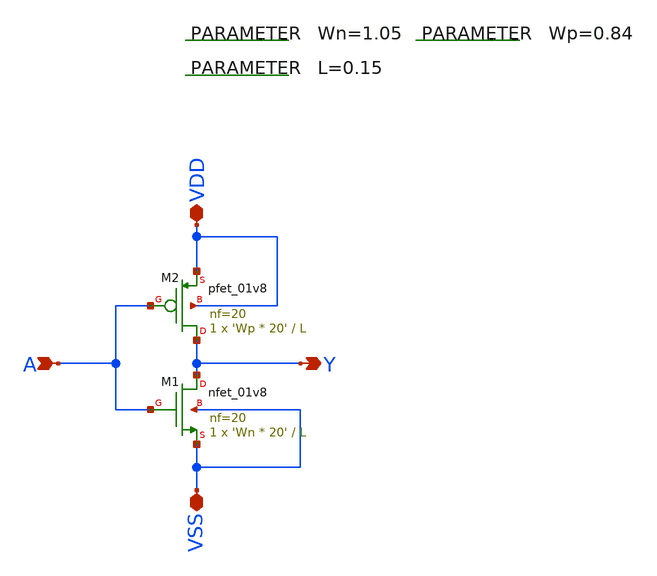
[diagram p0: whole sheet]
** sch_path: images/align/design/Examples/Inverter/inverter.sch
**.subckt inverter A Y VDD VSS
*.ipin A
*.opin Y
*.iopin VDD
*.iopin VSS
.param Wn=1.05
.param L=0.15
.param Wp=0.84
XM2 Y A VDD VDD sky130_fd_pr__pfet_01v8 L=L W='Wp * 20' nf=20 ad='int((nf+1)/2) * W/nf * 0.29' as='int((nf+2)/2) * W/nf * 0.29'
+ pd='2*int((nf+1)/2) * (W/nf + 0.29)' ps='2*int((nf+2)/2) * (W/nf + 0.29)' nrd='0.29 / W' nrs='0.29 / W'
+ sa=0 sb=0 sd=0 mult=1 m=1
XM1 Y A VSS VSS sky130_fd_pr__nfet_01v8 L=L W='Wn * 20' nf=20 ad='int((nf+1)/2) * W/nf * 0.29' as='int((nf+2)/2) * W/nf * 0.29'
+ pd='2*int((nf+1)/2) * (W/nf + 0.29)' ps='2*int((nf+2)/2) * (W/nf + 0.29)' nrd='0.29 / W' nrs='0.29 / W'
+ sa=0 sb=0 sd=0 mult=1 m=1
**.ends
.end
